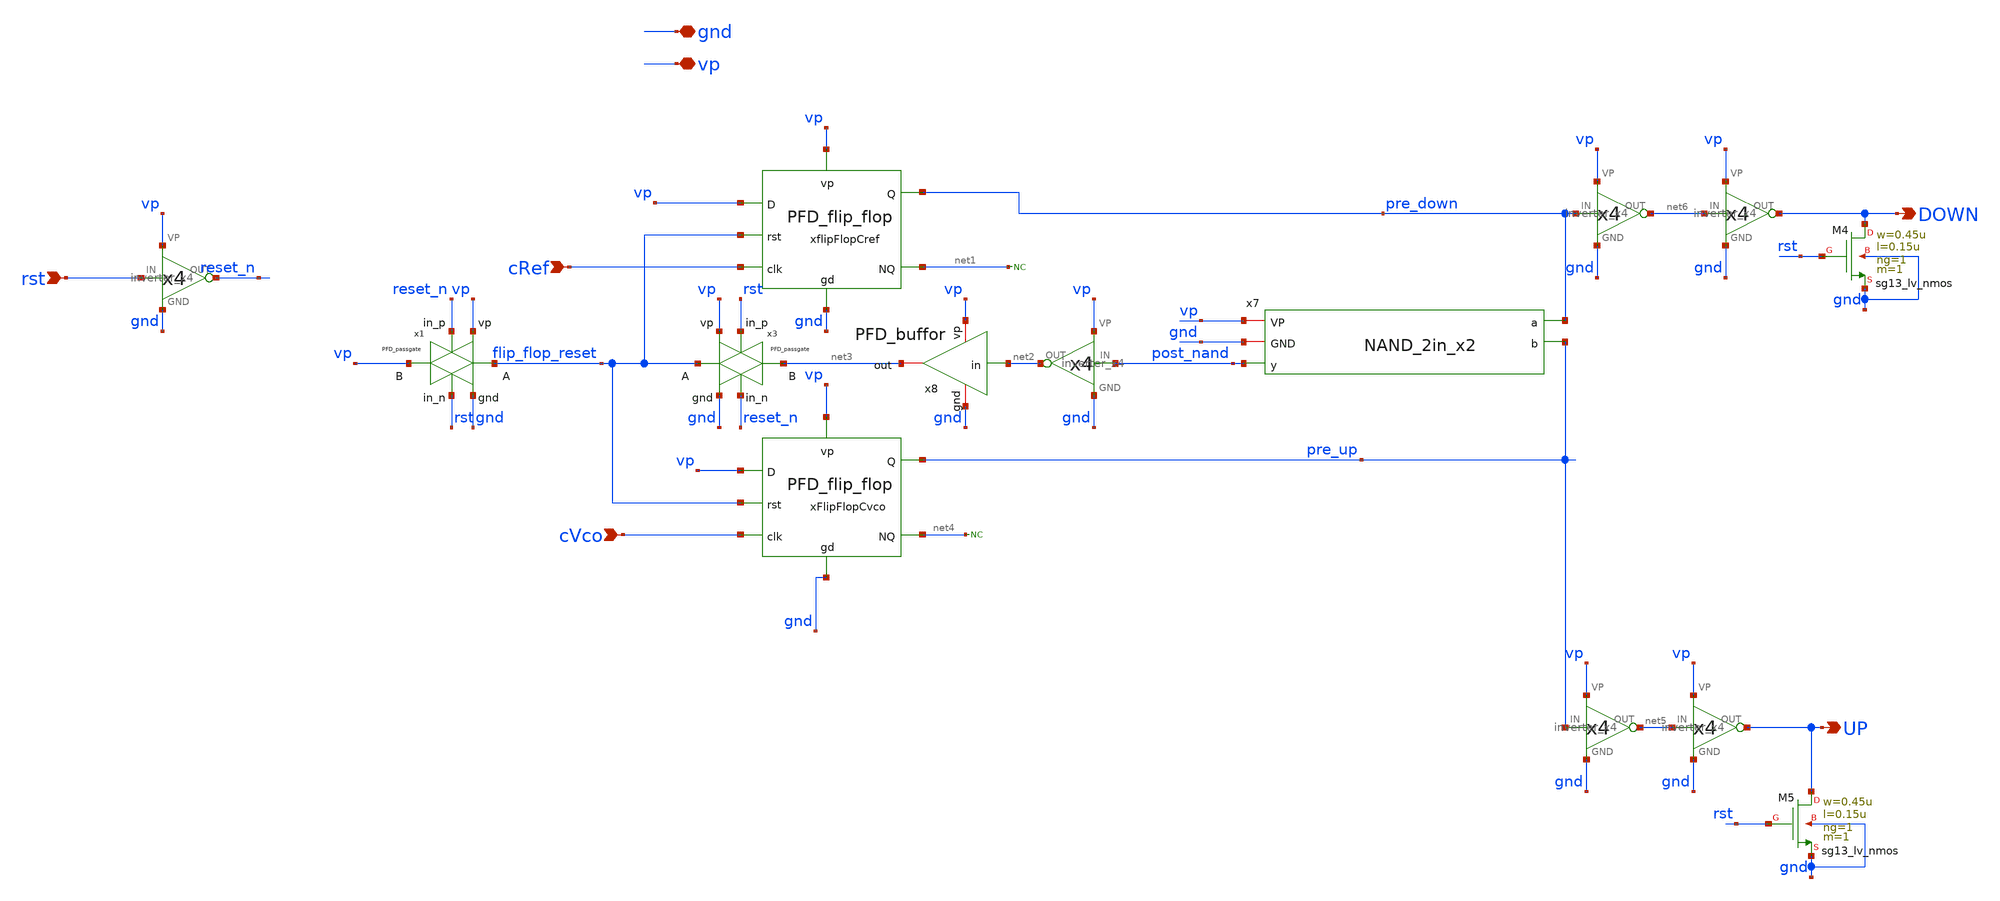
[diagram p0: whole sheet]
** sch_path: schematics/PFD/PFD_cell_2.sch
**.subckt PFD_cell_2 gnd vp cRef cVco rst UP DOWN
*.iopin gnd
*.iopin vp
*.ipin cRef
*.ipin cVco
*.ipin rst
*.opin UP
*.opin DOWN
* noconn #net1
* noconn #net4
x9 rst reset_n vp gnd inverter_x4
xflipFlopCref cRef flip_flop_reset vp pre_down net1 vp gnd PFD_flip_flop
xFlipFlopCvco cVco flip_flop_reset vp pre_up net4 vp gnd PFD_flip_flop
XM4 DOWN rst gnd gnd sg13_lv_nmos w=0.45u l=0.15u ng=1 m=1 mm_ok=1
XM5 UP rst gnd gnd sg13_lv_nmos w=0.45u l=0.15u ng=1 m=1 mm_ok=1
x4 net6 DOWN vp gnd inverter_x4
x6 net5 UP vp gnd inverter_x4
x2 pre_down net6 vp gnd inverter_x4
x5 pre_up net5 vp gnd inverter_x4
x1 rst vp flip_flop_reset vp gnd reset_n PFD_passgate
x3 reset_n vp flip_flop_reset net3 gnd rst PFD_passgate
x8 gnd vp net3 net2 PFD_buffor
x11 post_nand net2 vp gnd inverter_x4
x7 vp gnd pre_down post_nand pre_up NAND_2in_x2
**.ends
.end
